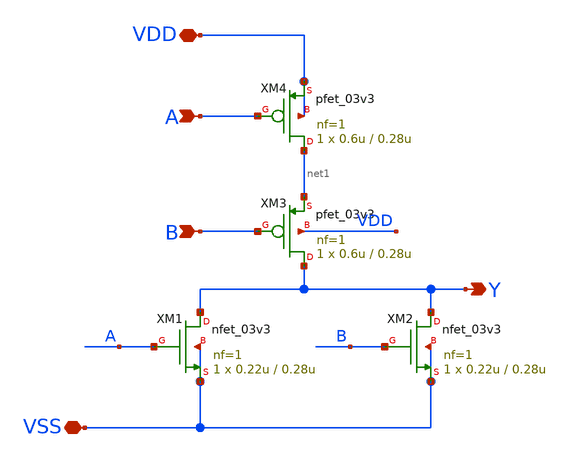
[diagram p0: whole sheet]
** sch_path: src/UN_PFD_GF180mcuD/UN_NOR0_GF180mcuD.sch
**.subckt UN_NOR0_GF180mcuD A B VDD VSS Y
*.ipin A
*.ipin B
*.iopin VDD
*.iopin VSS
*.opin Y
XM1 Y A VSS VSS nfet_03v3 L=0.28u W=0.22u nf=1 ad='int((nf+1)/2) * W/nf * 0.18u' as='int((nf+2)/2) * W/nf * 0.18u'
+ pd='2*int((nf+1)/2) * (W/nf + 0.18u)' ps='2*int((nf+2)/2) * (W/nf + 0.18u)' nrd='0.18u / W' nrs='0.18u / W'
+ sa=0 sb=0 sd=0 m=1
XM2 Y B VSS VSS nfet_03v3 L=0.28u W=0.22u nf=1 ad='int((nf+1)/2) * W/nf * 0.18u' as='int((nf+2)/2) * W/nf * 0.18u'
+ pd='2*int((nf+1)/2) * (W/nf + 0.18u)' ps='2*int((nf+2)/2) * (W/nf + 0.18u)' nrd='0.18u / W' nrs='0.18u / W'
+ sa=0 sb=0 sd=0 m=1
XM3 Y B net1 VDD pfet_03v3 L=0.28u W=0.6u nf=1 ad='int((nf+1)/2) * W/nf * 0.18u' as='int((nf+2)/2) * W/nf * 0.18u'
+ pd='2*int((nf+1)/2) * (W/nf + 0.18u)' ps='2*int((nf+2)/2) * (W/nf + 0.18u)' nrd='0.18u / W' nrs='0.18u / W'
+ sa=0 sb=0 sd=0 m=1
XM4 net1 A VDD VDD pfet_03v3 L=0.28u W=0.6u nf=1 ad='int((nf+1)/2) * W/nf * 0.18u' as='int((nf+2)/2) * W/nf * 0.18u'
+ pd='2*int((nf+1)/2) * (W/nf + 0.18u)' ps='2*int((nf+2)/2) * (W/nf + 0.18u)' nrd='0.18u / W' nrs='0.18u / W'
+ sa=0 sb=0 sd=0 m=1
**.ends
.end
